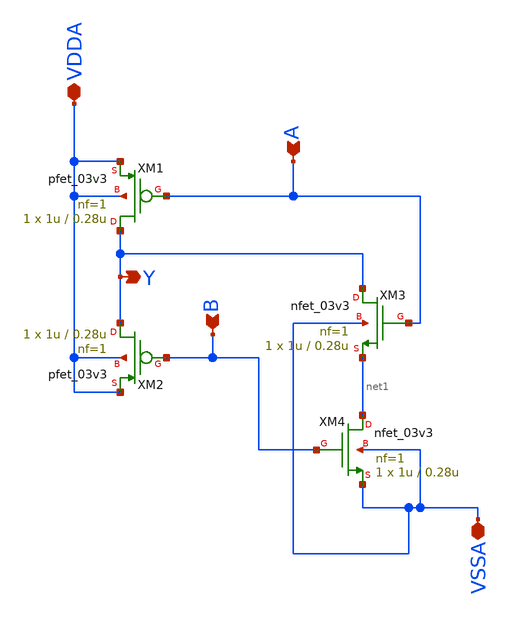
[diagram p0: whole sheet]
** sch_path: xschem/charge_pump/cp_nand.sch
**.subckt cp_nand VDDA A Y VSSA B
*.iopin VDDA
*.ipin A
*.opin Y
*.iopin VSSA
*.ipin B
XM1 Y A VDDA VDDA pfet_03v3 L=0.28u W=1u nf=1 ad='int((nf+1)/2) * W/nf * 0.18u' as='int((nf+2)/2) * W/nf * 0.18u'
+ pd='2*int((nf+1)/2) * (W/nf + 0.18u)' ps='2*int((nf+2)/2) * (W/nf + 0.18u)' nrd='0.18u / W' nrs='0.18u / W'
+ sa=0 sb=0 sd=0 m=1
XM2 Y B VDDA VDDA pfet_03v3 L=0.28u W=1u nf=1 ad='int((nf+1)/2) * W/nf * 0.18u' as='int((nf+2)/2) * W/nf * 0.18u'
+ pd='2*int((nf+1)/2) * (W/nf + 0.18u)' ps='2*int((nf+2)/2) * (W/nf + 0.18u)' nrd='0.18u / W' nrs='0.18u / W'
+ sa=0 sb=0 sd=0 m=1
XM3 Y A net1 VSSA nfet_03v3 L=0.28u W=1u nf=1 ad='int((nf+1)/2) * W/nf * 0.18u' as='int((nf+2)/2) * W/nf * 0.18u'
+ pd='2*int((nf+1)/2) * (W/nf + 0.18u)' ps='2*int((nf+2)/2) * (W/nf + 0.18u)' nrd='0.18u / W' nrs='0.18u / W'
+ sa=0 sb=0 sd=0 m=1
XM4 net1 B VSSA VSSA nfet_03v3 L=0.28u W=1u nf=1 ad='int((nf+1)/2) * W/nf * 0.18u' as='int((nf+2)/2) * W/nf * 0.18u'
+ pd='2*int((nf+1)/2) * (W/nf + 0.18u)' ps='2*int((nf+2)/2) * (W/nf + 0.18u)' nrd='0.18u / W' nrs='0.18u / W'
+ sa=0 sb=0 sd=0 m=1
**.ends
.end
